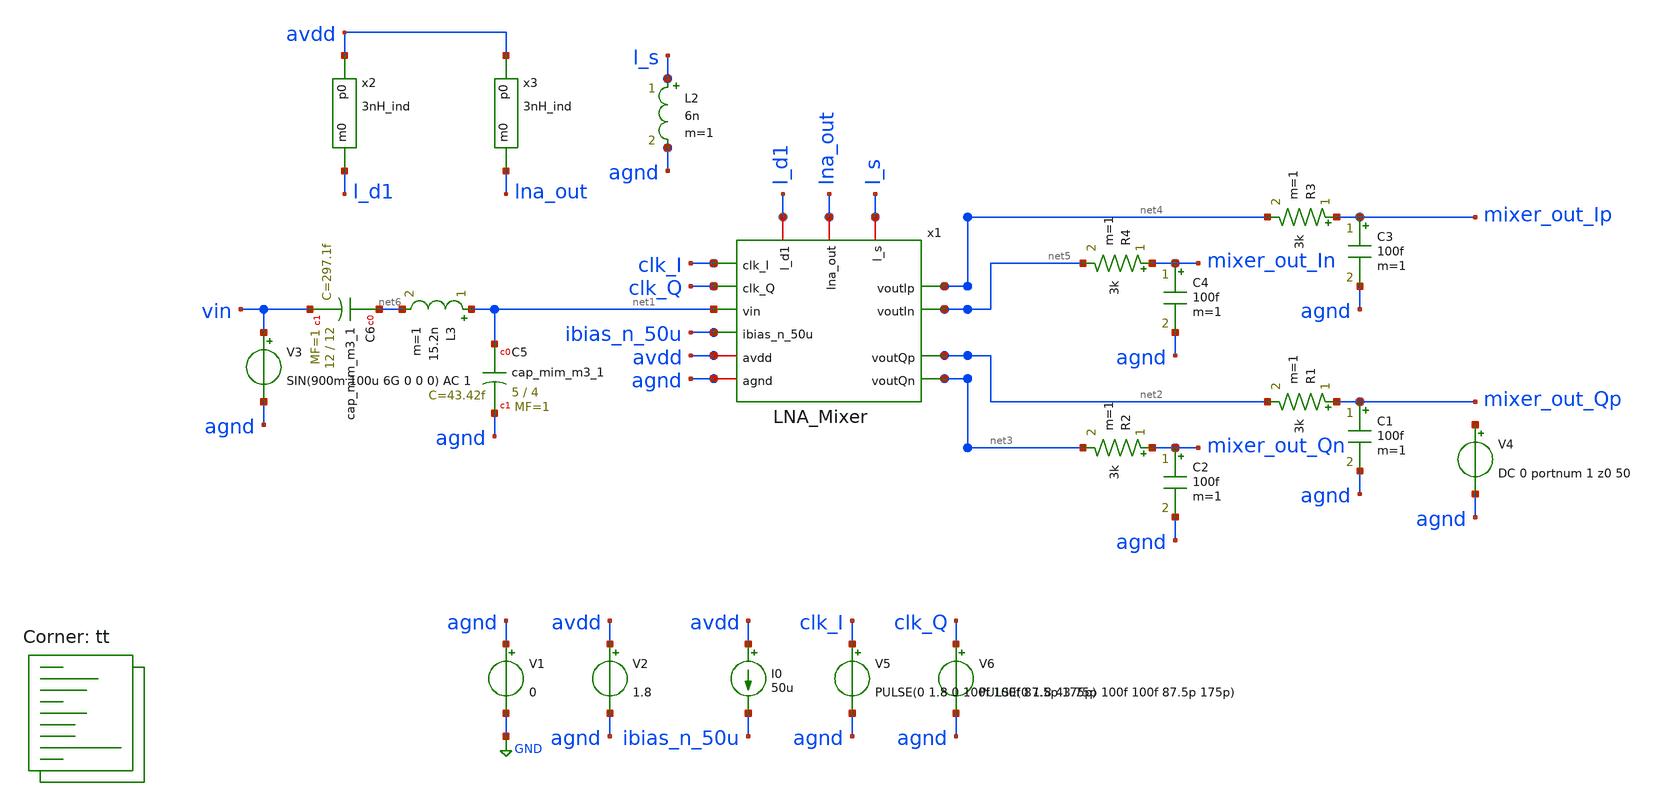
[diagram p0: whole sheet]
** sch_path: Testbenches/TB_LNA_Mixer.sch
**.subckt TB_LNA_Mixer
V1 agnd GND 0
V2 avdd agnd 1.8
V3 vin agnd SIN(900m 100u 6G 0 0 0) AC 1
V5 clk_I agnd PULSE(0 1.8 0 100f 100f 87.5p 175p)
V6 clk_Q agnd PULSE(0 1.8 43.75p 100f 100f 87.5p 175p)
R1 mixer_out_Qp net2 3k m=1
C1 mixer_out_Qp agnd 100f m=1
R2 mixer_out_Qn net3 3k m=1
C2 mixer_out_Qn agnd 100f m=1
R3 mixer_out_Ip net4 3k m=1
C3 mixer_out_Ip agnd 100f m=1
R4 mixer_out_In net5 3k m=1
C4 mixer_out_In agnd 100f m=1
I0 avdd ibias_n_50u 50u
L3 net1 net6 15.2n m=1
XC6 net6 vin sky130_fd_pr__cap_mim_m3_1 W=12 L=12 MF=1 m=1
L2 l_s agnd 6n m=1
V4 net7 agnd DC 0 portnum 1 z0 50
XC5 net1 agnd sky130_fd_pr__cap_mim_m3_1 W=5 L=4 MF=1 m=1
x1 lna_out net4 clk_I avdd ibias_n_50u net5 net1 agnd net2 l_s clk_Q net3 l_d1 LNA_Mixer
x2 avdd l_d1 3nH_ind
x3 avdd lna_out 3nH_ind
**** begin user architecture code


.include /foss/designs/EE437/Project/ee437-quantum-controller/LNA/3nH_ind.spice
.include /foss/designs/EE437/Project/ee437-quantum-controller/LNA/LNA_Mixer.pex.spice

.option savecurrents

.control
save all

op
write TB_LNA_Mixer.raw

* AC ANALYSIS *
set appendwrite
ac dec 1000 5e9 7e9
remzerovec
*let vgate_lna = v(x1.vgate)
let gain_lna = db(mag(v(lna_out) / v(vin)))
*let gain_gate = db(mag(v(lna_out) / v(vgate_lna)))
*let gain_total = db(mag(v(mixer_out_I) / v(vin)))
write TB_LNA_Mixer.raw

* TRANSIENT FOR TIME DOMAIN *
*set appendwrite
*tran 50p 100n
*let mixer_out_I = v(mixer_out_Ip) - v(mixer_out_In)
*let mixer_out_Q = v(mixer_out_Qp) - v(mixer_out_Qn)
*write TB_LNA_Mixer.raw

* TRANSIENT FOR FFT *
* (Set input freq to 77.819824e6) *
*set appendwrite
*tran 50p 5u
*let lin-tstart 0
*let lin-tstop 5u
*let lin-tstep 10p
*linearize V(mixer_out_I)
*fft V(mixer_out_I)
*let mixer_out_I_fft = mag(V(mixer_out_I))
*write TB_LNA_Mixer.raw

* S-PARAMETER / NF ANALYSIS *
*set appendwrite
*sp dec 1000 5e9 7e9 1
*let S11 = db(mag(v(s_1_1)))
*write TB_LNA_Mixer.raw

* NOISE ANALYSIS *
*set appendwrite
*noise v(mixer_out_I) V3 dec 1000 1 10e9
*setplot noise1
*set sqrnoise
*write TB_LNA_Mixer.raw

* DISTORTION ANALYSIS WIP *
*set appendwrite
*disto dec 1000 1 10e9
*write TB_LNA_Mixer.raw

.endc


.lib $::SKYWATER_MODELS/sky130.lib.spice tt
**** end user architecture code
**.ends
.GLOBAL GND
.end
